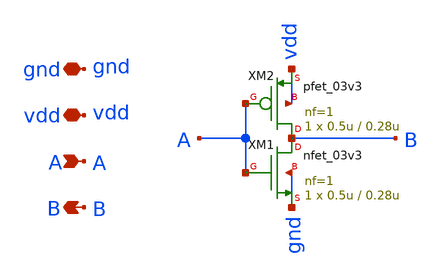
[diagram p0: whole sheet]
** sch_path: sim_postlayout/esquematicos/inversor_simbolo.sch
**.subckt inversor_simbolo A B gnd vdd
*.ipin A
*.opin B
*.iopin gnd
*.iopin vdd
XM1 B A gnd gnd nfet_03v3 L=0.28u W=0.5u nf=1 ad='int((nf+1)/2) * W/nf * 0.18u' as='int((nf+2)/2) * W/nf * 0.18u'
+ pd='2*int((nf+1)/2) * (W/nf + 0.18u)' ps='2*int((nf+2)/2) * (W/nf + 0.18u)' nrd='0.18u / W' nrs='0.18u / W'
+ sa=0 sb=0 sd=0 m=1 par=1
XM2 B A vdd vdd pfet_03v3 L=0.28u W=0.5u nf=1 ad='int((nf+1)/2) * W/nf * 0.18u' as='int((nf+2)/2) * W/nf * 0.18u'
+ pd='2*int((nf+1)/2) * (W/nf + 0.18u)' ps='2*int((nf+2)/2) * (W/nf + 0.18u)' nrd='0.18u / W' nrs='0.18u / W'
+ sa=0 sb=0 sd=0 m=1 par=1
**.ends
.end
